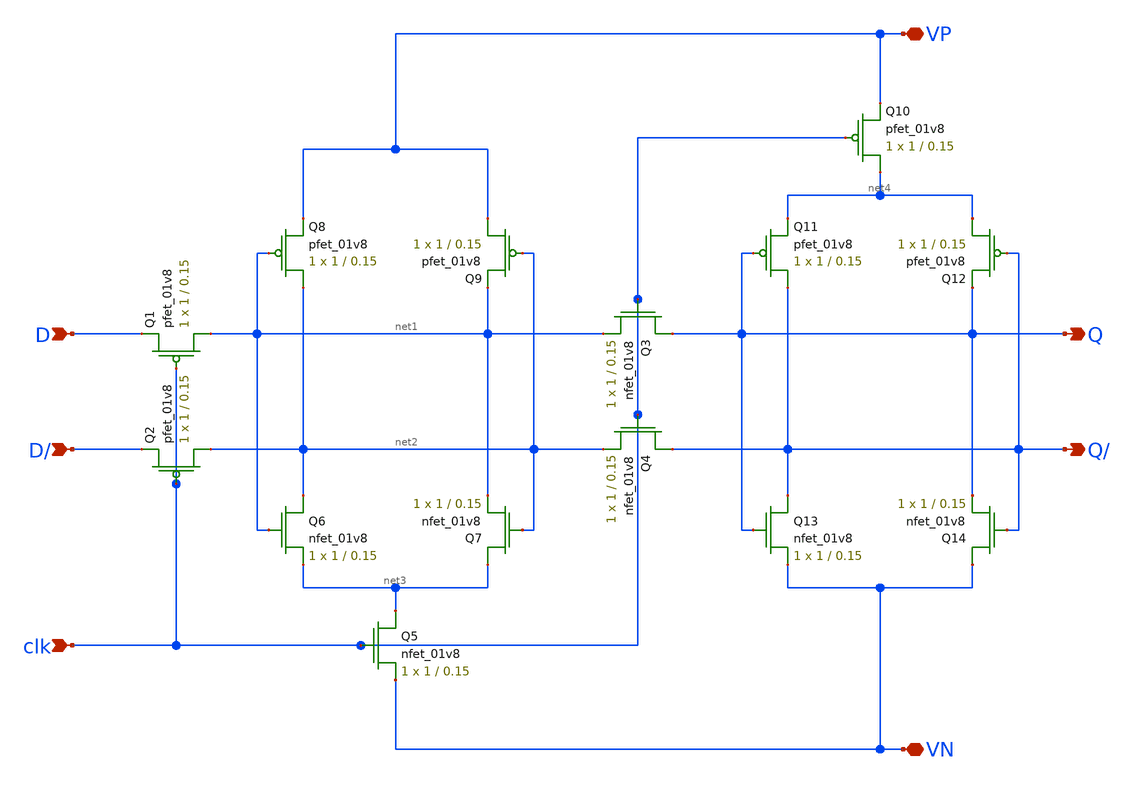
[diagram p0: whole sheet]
** sch_path: MADVLSI_MP2/Sil_CSRL.sch
**.subckt Sil_CSRL VN VP D D/ clk Q Q/
*.iopin VN
*.iopin VP
*.ipin D
*.ipin D/
*.ipin clk
*.opin Q
*.opin Q/
XQ1 net1 clk D VDD sky130_fd_pr__pfet_01v8 L=0.15 W=1 nf=1 ad='int((nf+1)/2) * W/nf * 0.29' as='int((nf+2)/2) * W/nf * 0.29'
+ pd='2*int((nf+1)/2) * (W/nf + 0.29)' ps='2*int((nf+2)/2) * (W/nf + 0.29)' nrd='0.29 / W' nrs='0.29 / W'
+ sa=0 sb=0 sd=0 mult=1 m=1
XQ2 net2 clk D/ VDD sky130_fd_pr__pfet_01v8 L=0.15 W=1 nf=1 ad='int((nf+1)/2) * W/nf * 0.29' as='int((nf+2)/2) * W/nf * 0.29'
+ pd='2*int((nf+1)/2) * (W/nf + 0.29)' ps='2*int((nf+2)/2) * (W/nf + 0.29)' nrd='0.29 / W' nrs='0.29 / W'
+ sa=0 sb=0 sd=0 mult=1 m=1
XQ3 Q clk net1 GND sky130_fd_pr__nfet_01v8 L=0.15 W=1 nf=1 ad='int((nf+1)/2) * W/nf * 0.29' as='int((nf+2)/2) * W/nf * 0.29'
+ pd='2*int((nf+1)/2) * (W/nf + 0.29)' ps='2*int((nf+2)/2) * (W/nf + 0.29)' nrd='0.29 / W' nrs='0.29 / W'
+ sa=0 sb=0 sd=0 mult=1 m=1
XQ4 Q/ clk net2 GND sky130_fd_pr__nfet_01v8 L=0.15 W=1 nf=1 ad='int((nf+1)/2) * W/nf * 0.29' as='int((nf+2)/2) * W/nf * 0.29'
+ pd='2*int((nf+1)/2) * (W/nf + 0.29)' ps='2*int((nf+2)/2) * (W/nf + 0.29)' nrd='0.29 / W' nrs='0.29 / W'
+ sa=0 sb=0 sd=0 mult=1 m=1
XQ5 net3 clk VN GND sky130_fd_pr__nfet_01v8 L=0.15 W=1 nf=1 ad='int((nf+1)/2) * W/nf * 0.29' as='int((nf+2)/2) * W/nf * 0.29'
+ pd='2*int((nf+1)/2) * (W/nf + 0.29)' ps='2*int((nf+2)/2) * (W/nf + 0.29)' nrd='0.29 / W' nrs='0.29 / W'
+ sa=0 sb=0 sd=0 mult=1 m=1
XQ6 net2 net1 net3 GND sky130_fd_pr__nfet_01v8 L=0.15 W=1 nf=1 ad='int((nf+1)/2) * W/nf * 0.29' as='int((nf+2)/2) * W/nf * 0.29'
+ pd='2*int((nf+1)/2) * (W/nf + 0.29)' ps='2*int((nf+2)/2) * (W/nf + 0.29)' nrd='0.29 / W' nrs='0.29 / W'
+ sa=0 sb=0 sd=0 mult=1 m=1
XQ7 net3 net2 net1 GND sky130_fd_pr__nfet_01v8 L=0.15 W=1 nf=1 ad='int((nf+1)/2) * W/nf * 0.29' as='int((nf+2)/2) * W/nf * 0.29'
+ pd='2*int((nf+1)/2) * (W/nf + 0.29)' ps='2*int((nf+2)/2) * (W/nf + 0.29)' nrd='0.29 / W' nrs='0.29 / W'
+ sa=0 sb=0 sd=0 mult=1 m=1
XQ8 net2 net1 VP VDD sky130_fd_pr__pfet_01v8 L=0.15 W=1 nf=1 ad='int((nf+1)/2) * W/nf * 0.29' as='int((nf+2)/2) * W/nf * 0.29'
+ pd='2*int((nf+1)/2) * (W/nf + 0.29)' ps='2*int((nf+2)/2) * (W/nf + 0.29)' nrd='0.29 / W' nrs='0.29 / W'
+ sa=0 sb=0 sd=0 mult=1 m=1
XQ9 VP net2 net1 VDD sky130_fd_pr__pfet_01v8 L=0.15 W=1 nf=1 ad='int((nf+1)/2) * W/nf * 0.29' as='int((nf+2)/2) * W/nf * 0.29'
+ pd='2*int((nf+1)/2) * (W/nf + 0.29)' ps='2*int((nf+2)/2) * (W/nf + 0.29)' nrd='0.29 / W' nrs='0.29 / W'
+ sa=0 sb=0 sd=0 mult=1 m=1
XQ13 Q/ Q VN GND sky130_fd_pr__nfet_01v8 L=0.15 W=1 nf=1 ad='int((nf+1)/2) * W/nf * 0.29' as='int((nf+2)/2) * W/nf * 0.29'
+ pd='2*int((nf+1)/2) * (W/nf + 0.29)' ps='2*int((nf+2)/2) * (W/nf + 0.29)' nrd='0.29 / W' nrs='0.29 / W'
+ sa=0 sb=0 sd=0 mult=1 m=1
XQ14 VN Q/ Q GND sky130_fd_pr__nfet_01v8 L=0.15 W=1 nf=1 ad='int((nf+1)/2) * W/nf * 0.29' as='int((nf+2)/2) * W/nf * 0.29'
+ pd='2*int((nf+1)/2) * (W/nf + 0.29)' ps='2*int((nf+2)/2) * (W/nf + 0.29)' nrd='0.29 / W' nrs='0.29 / W'
+ sa=0 sb=0 sd=0 mult=1 m=1
XQ11 Q/ Q net4 VDD sky130_fd_pr__pfet_01v8 L=0.15 W=1 nf=1 ad='int((nf+1)/2) * W/nf * 0.29' as='int((nf+2)/2) * W/nf * 0.29'
+ pd='2*int((nf+1)/2) * (W/nf + 0.29)' ps='2*int((nf+2)/2) * (W/nf + 0.29)' nrd='0.29 / W' nrs='0.29 / W'
+ sa=0 sb=0 sd=0 mult=1 m=1
XQ12 net4 Q/ Q VDD sky130_fd_pr__pfet_01v8 L=0.15 W=1 nf=1 ad='int((nf+1)/2) * W/nf * 0.29' as='int((nf+2)/2) * W/nf * 0.29'
+ pd='2*int((nf+1)/2) * (W/nf + 0.29)' ps='2*int((nf+2)/2) * (W/nf + 0.29)' nrd='0.29 / W' nrs='0.29 / W'
+ sa=0 sb=0 sd=0 mult=1 m=1
XQ10 net4 clk VP VDD sky130_fd_pr__pfet_01v8 L=0.15 W=1 nf=1 ad='int((nf+1)/2) * W/nf * 0.29' as='int((nf+2)/2) * W/nf * 0.29'
+ pd='2*int((nf+1)/2) * (W/nf + 0.29)' ps='2*int((nf+2)/2) * (W/nf + 0.29)' nrd='0.29 / W' nrs='0.29 / W'
+ sa=0 sb=0 sd=0 mult=1 m=1
**.ends
.end
